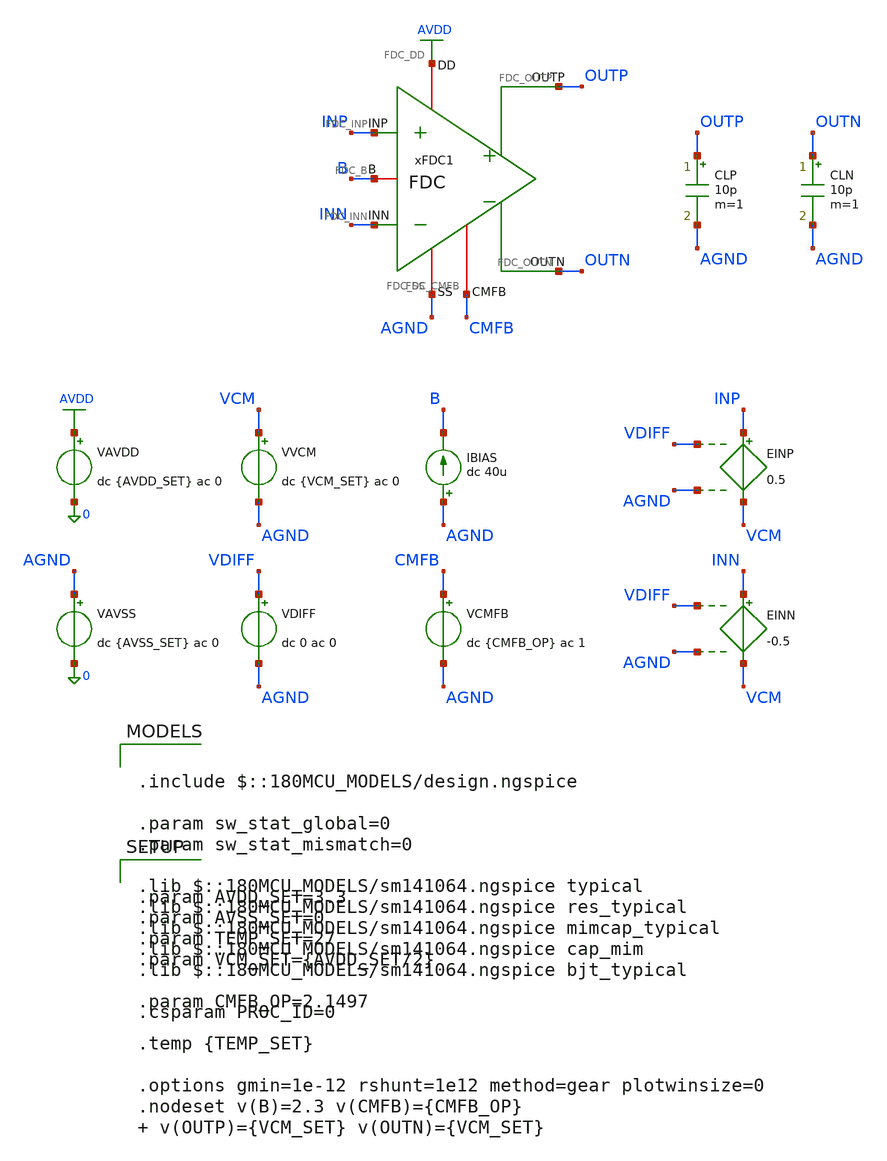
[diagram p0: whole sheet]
** sch_path: Design_Files/IC Design/Testbench/ANALOG_BLOCKS/FD_OTA/FDC/Open_Loop/FDC_TB_PLANT_NOM.sch
**.subckt FDC_TB_PLANT_NOM
IBIAS AGND B dc 40u
VAVDD AVDD 0 dc {AVDD_SET} ac 0
.save i(vavdd)
CLP OUTP AGND 10p m=1
VVCM VCM AGND dc {VCM_SET} ac 0
VDIFF VDIFF AGND dc 0 ac 0
VAVSS AGND 0 dc {AVSS_SET} ac 0
.save i(vavss)
EINN INN VCM VDIFF AGND -0.5
EINP INP VCM VDIFF AGND 0.5
CLN OUTN AGND 10p m=1
VCMFB CMFB AGND dc {CMFB_OP} ac 1
xFDC1 AVDD AGND INP INN OUTN B OUTP CMFB FDC
**** begin user architecture code

.include $::180MCU_MODELS/design.ngspice

.param sw_stat_global=0
.param sw_stat_mismatch=0

.lib $::180MCU_MODELS/sm141064.ngspice typical
.lib $::180MCU_MODELS/sm141064.ngspice res_typical
.lib $::180MCU_MODELS/sm141064.ngspice mimcap_typical
.lib $::180MCU_MODELS/sm141064.ngspice cap_mim
.lib $::180MCU_MODELS/sm141064.ngspice bjt_typical

.csparam PROC_ID=0



.control
destroy all
save all
set wr_vecnames
set wr_singlescale
option numdgt=15

shell mkdir -p
+ /foss/designs/ECG_Acquisition_IC/Measurement_Results/IC_Simulation/ANALOG_BLOCKS/FD_OTA/FDC/NOM.Result_txt

shell rm -f
+ /foss/designs/ECG_Acquisition_IC/Measurement_Results/IC_Simulation/ANALOG_BLOCKS/FD_OTA/FDC/NOM.Result_txt/NOM.plant_ac.txt

alter @VAVDD[ACMAG]  = 0
alter @VAVSS[ACMAG]  = 0
alter @VVCM[ACMAG]   = 0
alter @VDIFF[ACMAG]  = 0

alter @VCMFB[ACMAG]   = 1
alter @VCMFB[ACPHASE] = 0

ac dec 200 0.1 1G

let vcmfb_ac  = v(cmfb)-v(agnd)
let voutp_ac  = v(outp)-v(agnd)
let voutn_ac  = v(outn)-v(agnd)
let voutcm_ac = (voutp_ac+voutn_ac)/2

let plant_ac   = voutcm_ac/vcmfb_ac
let plant_real = real(plant_ac)
let plant_imag = imag(plant_ac)

setscale frequency

wrdata
+ /foss/designs/ECG_Acquisition_IC/Measurement_Results/IC_Simulation/ANALOG_BLOCKS/FD_OTA/FDC/NOM.Result_txt/NOM.plant_ac.txt plant_real plant_imag

quit
.endc




.param AVDD_SET=3.3
.param AVSS_SET=0
.param TEMP_SET=27
.param VCM_SET={AVDD_SET/2}

.param CMFB_OP=2.1497

.temp {TEMP_SET}

.options gmin=1e-12 rshunt=1e12 method=gear plotwinsize=0
.nodeset v(B)=2.3 v(CMFB)={CMFB_OP}  v(OUTP)={VCM_SET} v(OUTN)={VCM_SET}


**** end user architecture code
**.ends
.GLOBAL AVDD
.end
